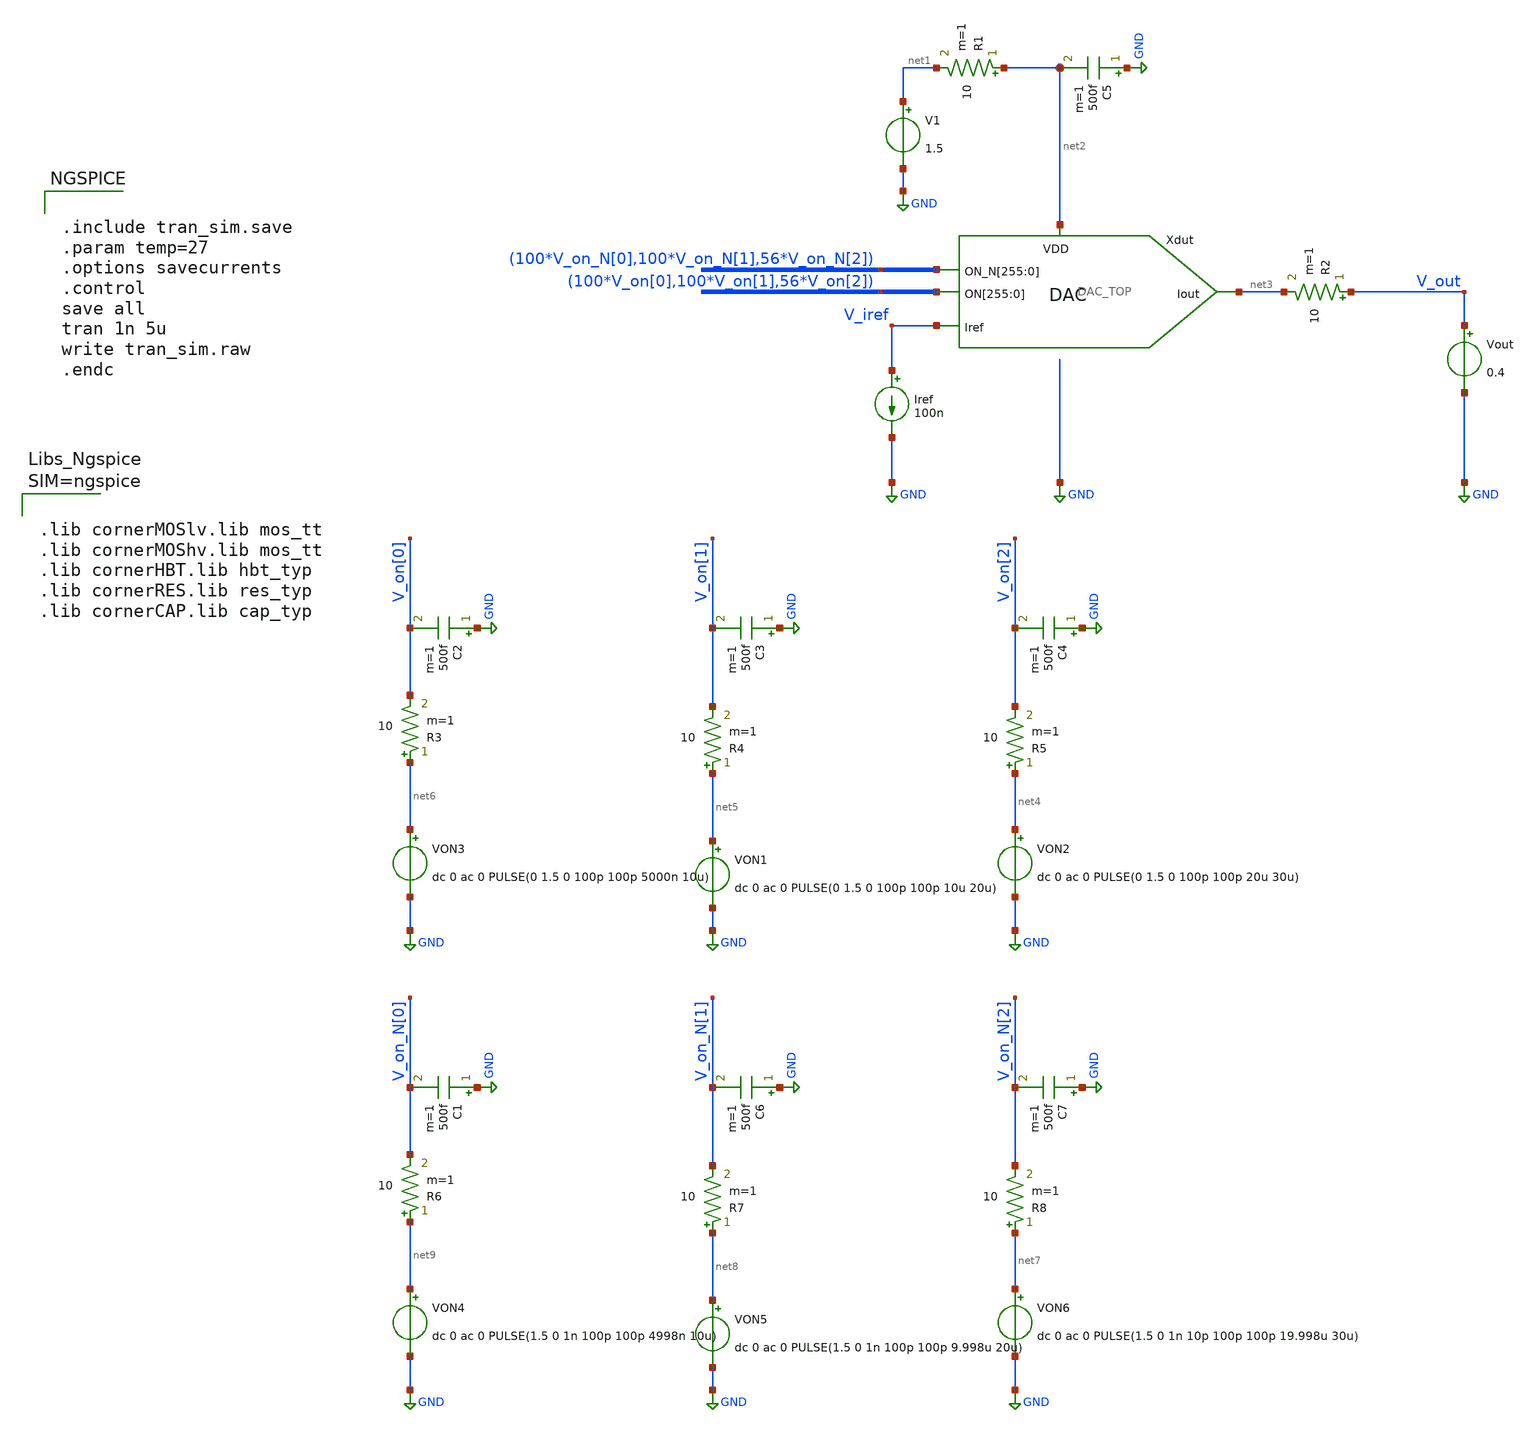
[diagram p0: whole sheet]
** sch_path: xschem/tran_sim.sch
**.subckt tran_sim
Xdut net2 V_on[0] V_on[0] V_on[0] V_on[0] V_on[0] V_on[0] V_on[0] V_on[0] V_on[0] V_on[0] V_on[0]
+ V_on[0] V_on[0] V_on[0] V_on[0] V_on[0] V_on[0] V_on[0] V_on[0] V_on[0] V_on[0] V_on[0] V_on[0] V_on[0]
+ V_on[0] V_on[0] V_on[0] V_on[0] V_on[0] V_on[0] V_on[0] V_on[0] V_on[0] V_on[0] V_on[0] V_on[0] V_on[0]
+ V_on[0] V_on[0] V_on[0] V_on[0] V_on[0] V_on[0] V_on[0] V_on[0] V_on[0] V_on[0] V_on[0] V_on[0] V_on[0]
+ V_on[0] V_on[0] V_on[0] V_on[0] V_on[0] V_on[0] V_on[0] V_on[0] V_on[0] V_on[0] V_on[0] V_on[0] V_on[0]
+ V_on[0] V_on[0] V_on[0] V_on[0] V_on[0] V_on[0] V_on[0] V_on[0] V_on[0] V_on[0] V_on[0] V_on[0] V_on[0]
+ V_on[0] V_on[0] V_on[0] V_on[0] V_on[0] V_on[0] V_on[0] V_on[0] V_on[0] V_on[0] V_on[0] V_on[0] V_on[0]
+ V_on[0] V_on[0] V_on[0] V_on[0] V_on[0] V_on[0] V_on[0] V_on[0] V_on[0] V_on[0] V_on[0] V_on[1] V_on[1]
+ V_on[1] V_on[1] V_on[1] V_on[1] V_on[1] V_on[1] V_on[1] V_on[1] V_on[1] V_on[1] V_on[1] V_on[1] V_on[1]
+ V_on[1] V_on[1] V_on[1] V_on[1] V_on[1] V_on[1] V_on[1] V_on[1] V_on[1] V_on[1] V_on[1] V_on[1] V_on[1]
+ V_on[1] V_on[1] V_on[1] V_on[1] V_on[1] V_on[1] V_on[1] V_on[1] V_on[1] V_on[1] V_on[1] V_on[1] V_on[1]
+ V_on[1] V_on[1] V_on[1] V_on[1] V_on[1] V_on[1] V_on[1] V_on[1] V_on[1] V_on[1] V_on[1] V_on[1] V_on[1]
+ V_on[1] V_on[1] V_on[1] V_on[1] V_on[1] V_on[1] V_on[1] V_on[1] V_on[1] V_on[1] V_on[1] V_on[1] V_on[1]
+ V_on[1] V_on[1] V_on[1] V_on[1] V_on[1] V_on[1] V_on[1] V_on[1] V_on[1] V_on[1] V_on[1] V_on[1] V_on[1]
+ V_on[1] V_on[1] V_on[1] V_on[1] V_on[1] V_on[1] V_on[1] V_on[1] V_on[1] V_on[1] V_on[1] V_on[1] V_on[1]
+ V_on[1] V_on[1] V_on[1] V_on[1] V_on[1] V_on[1] V_on[1] V_on[2] V_on[2] V_on[2] V_on[2] V_on[2] V_on[2]
+ V_on[2] V_on[2] V_on[2] V_on[2] V_on[2] V_on[2] V_on[2] V_on[2] V_on[2] V_on[2] V_on[2] V_on[2] V_on[2]
+ V_on[2] V_on[2] V_on[2] V_on[2] V_on[2] V_on[2] V_on[2] V_on[2] V_on[2] V_on[2] V_on[2] V_on[2] V_on[2]
+ V_on[2] V_on[2] V_on[2] V_on[2] V_on[2] V_on[2] V_on[2] V_on[2] V_on[2] V_on[2] V_on[2] V_on[2] V_on[2]
+ V_on[2] V_on[2] V_on[2] V_on[2] V_on[2] V_on[2] V_on[2] V_on[2] V_on[2] V_on[2] V_on[2] net3 V_iref
+ V_on_N[0] V_on_N[0] V_on_N[0] V_on_N[0] V_on_N[0] V_on_N[0] V_on_N[0] V_on_N[0] V_on_N[0] V_on_N[0] V_on_N[0]
+ V_on_N[0] V_on_N[0] V_on_N[0] V_on_N[0] V_on_N[0] V_on_N[0] V_on_N[0] V_on_N[0] V_on_N[0] V_on_N[0] V_on_N[0]
+ V_on_N[0] V_on_N[0] V_on_N[0] V_on_N[0] V_on_N[0] V_on_N[0] V_on_N[0] V_on_N[0] V_on_N[0] V_on_N[0] V_on_N[0]
+ V_on_N[0] V_on_N[0] V_on_N[0] V_on_N[0] V_on_N[0] V_on_N[0] V_on_N[0] V_on_N[0] V_on_N[0] V_on_N[0] V_on_N[0]
+ V_on_N[0] V_on_N[0] V_on_N[0] V_on_N[0] V_on_N[0] V_on_N[0] V_on_N[0] V_on_N[0] V_on_N[0] V_on_N[0] V_on_N[0]
+ V_on_N[0] V_on_N[0] V_on_N[0] V_on_N[0] V_on_N[0] V_on_N[0] V_on_N[0] V_on_N[0] V_on_N[0] V_on_N[0] V_on_N[0]
+ V_on_N[0] V_on_N[0] V_on_N[0] V_on_N[0] V_on_N[0] V_on_N[0] V_on_N[0] V_on_N[0] V_on_N[0] V_on_N[0] V_on_N[0]
+ V_on_N[0] V_on_N[0] V_on_N[0] V_on_N[0] V_on_N[0] V_on_N[0] V_on_N[0] V_on_N[0] V_on_N[0] V_on_N[0] V_on_N[0]
+ V_on_N[0] V_on_N[0] V_on_N[0] V_on_N[0] V_on_N[0] V_on_N[0] V_on_N[0] V_on_N[0] V_on_N[0] V_on_N[0] V_on_N[0]
+ V_on_N[0] V_on_N[1] V_on_N[1] V_on_N[1] V_on_N[1] V_on_N[1] V_on_N[1] V_on_N[1] V_on_N[1] V_on_N[1] V_on_N[1]
+ V_on_N[1] V_on_N[1] V_on_N[1] V_on_N[1] V_on_N[1] V_on_N[1] V_on_N[1] V_on_N[1] V_on_N[1] V_on_N[1] V_on_N[1]
+ V_on_N[1] V_on_N[1] V_on_N[1] V_on_N[1] V_on_N[1] V_on_N[1] V_on_N[1] V_on_N[1] V_on_N[1] V_on_N[1] V_on_N[1]
+ V_on_N[1] V_on_N[1] V_on_N[1] V_on_N[1] V_on_N[1] V_on_N[1] V_on_N[1] V_on_N[1] V_on_N[1] V_on_N[1] V_on_N[1]
+ V_on_N[1] V_on_N[1] V_on_N[1] V_on_N[1] V_on_N[1] V_on_N[1] V_on_N[1] V_on_N[1] V_on_N[1] V_on_N[1] V_on_N[1]
+ V_on_N[1] V_on_N[1] V_on_N[1] V_on_N[1] V_on_N[1] V_on_N[1] V_on_N[1] V_on_N[1] V_on_N[1] V_on_N[1] V_on_N[1]
+ V_on_N[1] V_on_N[1] V_on_N[1] V_on_N[1] V_on_N[1] V_on_N[1] V_on_N[1] V_on_N[1] V_on_N[1] V_on_N[1] V_on_N[1]
+ V_on_N[1] V_on_N[1] V_on_N[1] V_on_N[1] V_on_N[1] V_on_N[1] V_on_N[1] V_on_N[1] V_on_N[1] V_on_N[1] V_on_N[1]
+ V_on_N[1] V_on_N[1] V_on_N[1] V_on_N[1] V_on_N[1] V_on_N[1] V_on_N[1] V_on_N[1] V_on_N[1] V_on_N[1] V_on_N[1]
+ V_on_N[1] V_on_N[1] V_on_N[2] V_on_N[2] V_on_N[2] V_on_N[2] V_on_N[2] V_on_N[2] V_on_N[2] V_on_N[2] V_on_N[2]
+ V_on_N[2] V_on_N[2] V_on_N[2] V_on_N[2] V_on_N[2] V_on_N[2] V_on_N[2] V_on_N[2] V_on_N[2] V_on_N[2] V_on_N[2]
+ V_on_N[2] V_on_N[2] V_on_N[2] V_on_N[2] V_on_N[2] V_on_N[2] V_on_N[2] V_on_N[2] V_on_N[2] V_on_N[2] V_on_N[2]
+ V_on_N[2] V_on_N[2] V_on_N[2] V_on_N[2] V_on_N[2] V_on_N[2] V_on_N[2] V_on_N[2] V_on_N[2] V_on_N[2] V_on_N[2]
+ V_on_N[2] V_on_N[2] V_on_N[2] V_on_N[2] V_on_N[2] V_on_N[2] V_on_N[2] V_on_N[2] V_on_N[2] V_on_N[2] V_on_N[2]
+ V_on_N[2] V_on_N[2] V_on_N[2] DAC_TOP
V1 net1 GND 1.5
.save i(v1)
Vout V_out GND 0.4
.save i(vout)
Iref V_iref GND 100n
VON3 net6 GND dc 0 ac 0 PULSE(0 1.5 0 100p 100p 5000n 10u)
.save i(von3)
VON1 net5 GND dc 0 ac 0 PULSE(0 1.5 0 100p 100p 10u 20u)
.save i(von1)
VON2 net4 GND dc 0 ac 0 PULSE(0 1.5 0 100p 100p 20u 30u)
.save i(von2)
R1 net2 net1 10 m=1
R2 V_out net3 10 m=1
R3 net6 V_on[0] 10 m=1
R4 net5 V_on[1] 10 m=1
R5 net4 V_on[2] 10 m=1
C2 GND V_on[0] 500f m=1
C3 GND V_on[1] 500f m=1
C4 GND V_on[2] 500f m=1
C5 GND net2 500f m=1
VON4 net9 GND dc 0 ac 0 PULSE(1.5 0 1n 100p 100p 4998n 10u)
.save i(von4)
VON5 net8 GND dc 0 ac 0 PULSE(1.5 0 1n 100p 100p 9.998u 20u)
.save i(von5)
VON6 net7 GND dc 0 ac 0 PULSE(1.5 0 1n 10p 100p 100p 19.998u 30u)
.save i(von6)
R6 net9 V_on_N[0] 10 m=1
R7 net8 V_on_N[1] 10 m=1
R8 net7 V_on_N[2] 10 m=1
C1 GND V_on_N[0] 500f m=1
C6 GND V_on_N[1] 500f m=1
C7 GND V_on_N[2] 500f m=1
**** begin user architecture code


.include tran_sim.save
.param temp=27
.options savecurrents
.control
save all
tran 1n 5u
write tran_sim.raw
.endc





.lib cornerMOSlv.lib mos_tt
.lib cornerMOShv.lib mos_tt
.lib cornerHBT.lib hbt_typ
.lib cornerRES.lib res_typ
.lib cornerCAP.lib cap_typ



**** end user architecture code
**.ends
.GLOBAL GND
.end
